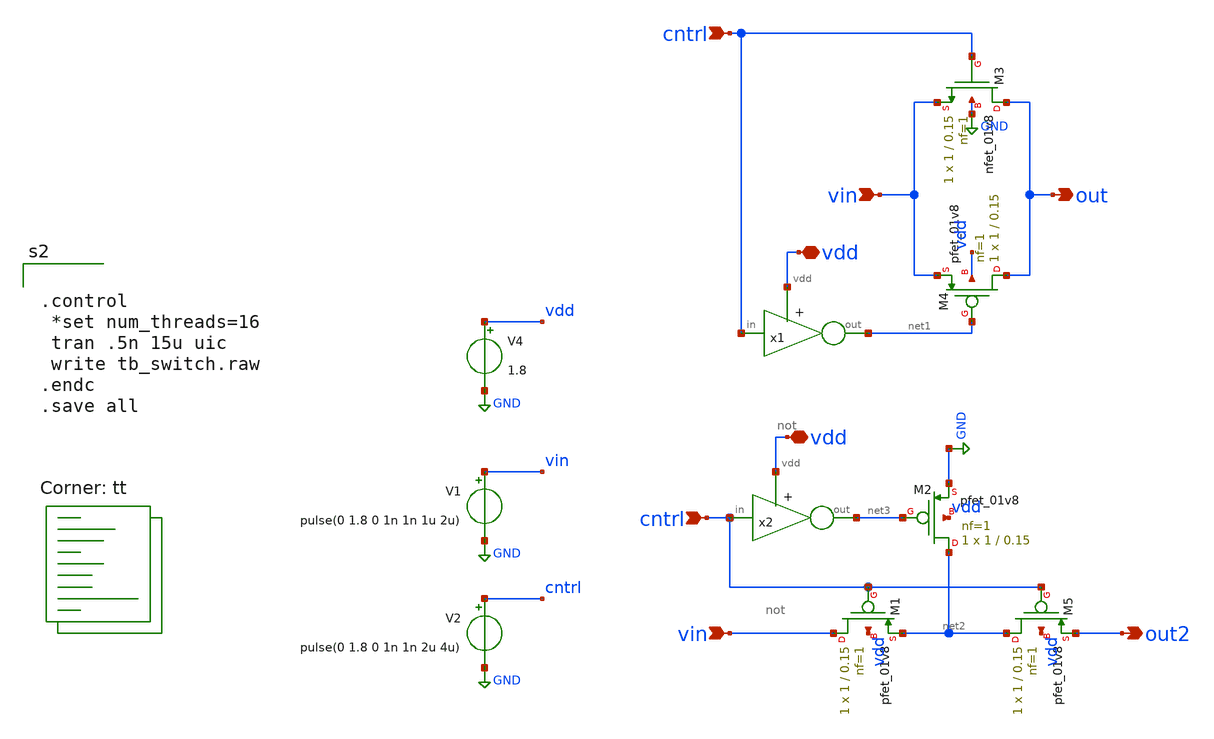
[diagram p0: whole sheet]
** sch_path: designs/subcells/tb_switch/tb_switch.sch
**.subckt tb_switch cntrl vin vdd out cntrl vin vdd out2
*.ipin cntrl
*.ipin vin
*.iopin vdd
*.opin out
*.ipin cntrl
*.ipin vin
*.iopin vdd
*.opin out2
V4 vdd GND 1.8
V1 vin GND pulse(0 1.8 0 1n 1n 1u 2u)
XM3 out cntrl vin GND sky130_fd_pr__nfet_01v8 L=0.15 W=1 nf=1 ad='int((1 + 1)/2) * 1 / 1 * 0.29' as='int((1 + 2)/2) * 1 / 1 * 0.29'
+ pd='2*int((1 + 1)/2) * (1 / 1 + 0.29)' ps='2*int((1 + 2)/2) * (1 / 1 + 0.29)' nrd='0.29 / 1 ' nrs='0.29 / 1 '
+ sa=0 sb=0 sd=0 mult=1 m=1
XM4 out net1 vin vdd sky130_fd_pr__pfet_01v8 L=0.15 W=1 nf=1 ad='int((nf+1)/2) * W/nf * 0.29' as='int((nf+2)/2) * W/nf * 0.29'
+ pd='2*int((nf+1)/2) * (W/nf + 0.29)' ps='2*int((nf+2)/2) * (W/nf + 0.29)' nrd='0.29 / W' nrs='0.29 / W'
+ sa=0 sb=0 sd=0 mult=1 m=1
x1 vdd cntrl net1 not
x2 vdd cntrl net3 not
V2 cntrl GND pulse(0 1.8 0 1n 1n 2u 4u)
XM2 net2 net3 GND vdd sky130_fd_pr__pfet_01v8 L=0.15 W=1 nf=1 ad='int((nf+1)/2) * W/nf * 0.29' as='int((nf+2)/2) * W/nf * 0.29'
+ pd='2*int((nf+1)/2) * (W/nf + 0.29)' ps='2*int((nf+2)/2) * (W/nf + 0.29)' nrd='0.29 / W' nrs='0.29 / W'
+ sa=0 sb=0 sd=0 mult=1 m=1
XM1 vin cntrl net2 vdd sky130_fd_pr__pfet_01v8 L=0.15 W=1 nf=1 ad='int((nf+1)/2) * W/nf * 0.29' as='int((nf+2)/2) * W/nf * 0.29'
+ pd='2*int((nf+1)/2) * (W/nf + 0.29)' ps='2*int((nf+2)/2) * (W/nf + 0.29)' nrd='0.29 / W' nrs='0.29 / W'
+ sa=0 sb=0 sd=0 mult=1 m=1
XM5 net2 cntrl out2 vdd sky130_fd_pr__pfet_01v8 L=0.15 W=1 nf=1 ad='int((nf+1)/2) * W/nf * 0.29' as='int((nf+2)/2) * W/nf * 0.29'
+ pd='2*int((nf+1)/2) * (W/nf + 0.29)' ps='2*int((nf+2)/2) * (W/nf + 0.29)' nrd='0.29 / W' nrs='0.29 / W'
+ sa=0 sb=0 sd=0 mult=1 m=1
**** begin user architecture code


.control
 *set num_threads=16
 tran .5n 15u uic
 write tb_switch.raw
.endc
.save all

.lib $::SKYWATER_MODELS/sky130.lib.spice tt
**** end user architecture code
**.ends

* expanding   symbol:  /foss/designs/spike_130/designs/subcells/core_not/not.sym # of pins=3
** sym_path: designs/subcells/core_not/not.sym
** sch_path: designs/subcells/core_not/not.sch
.subckt not vdd in out
*.ipin in
*.opin out
*.iopin vdd
XM10 out in vdd vdd sky130_fd_pr__pfet_01v8_lvt L=0.35 W=1 nf=1 ad='int((1 + 1)/2) * 1 / 1 * 0.29' as='int((1 + 2)/2) * 1 / 1 * 0.29'
+ pd='2*int((1 + 1)/2) * (1 / 1 + 0.29)' ps='2*int((1 + 2)/2) * (1 / 1 + 0.29)' nrd='0.29 / 1 ' nrs='0.29 / 1 '
+ sa=0 sb=0 sd=0 mult=1 m=1
XM1 out in GND GND sky130_fd_pr__nfet_01v8_lvt L=0.15 W=1 nf=1 ad='int((1 + 1)/2) * 1 / 1 * 0.29' as='int((1 + 2)/2) * 1 / 1 * 0.29'
+ pd='2*int((1 + 1)/2) * (1 / 1 + 0.29)' ps='2*int((1 + 2)/2) * (1 / 1 + 0.29)' nrd='0.29 / 1 ' nrs='0.29 / 1 '
+ sa=0 sb=0 sd=0 mult=1 m=1
.ends

.GLOBAL GND
.end
